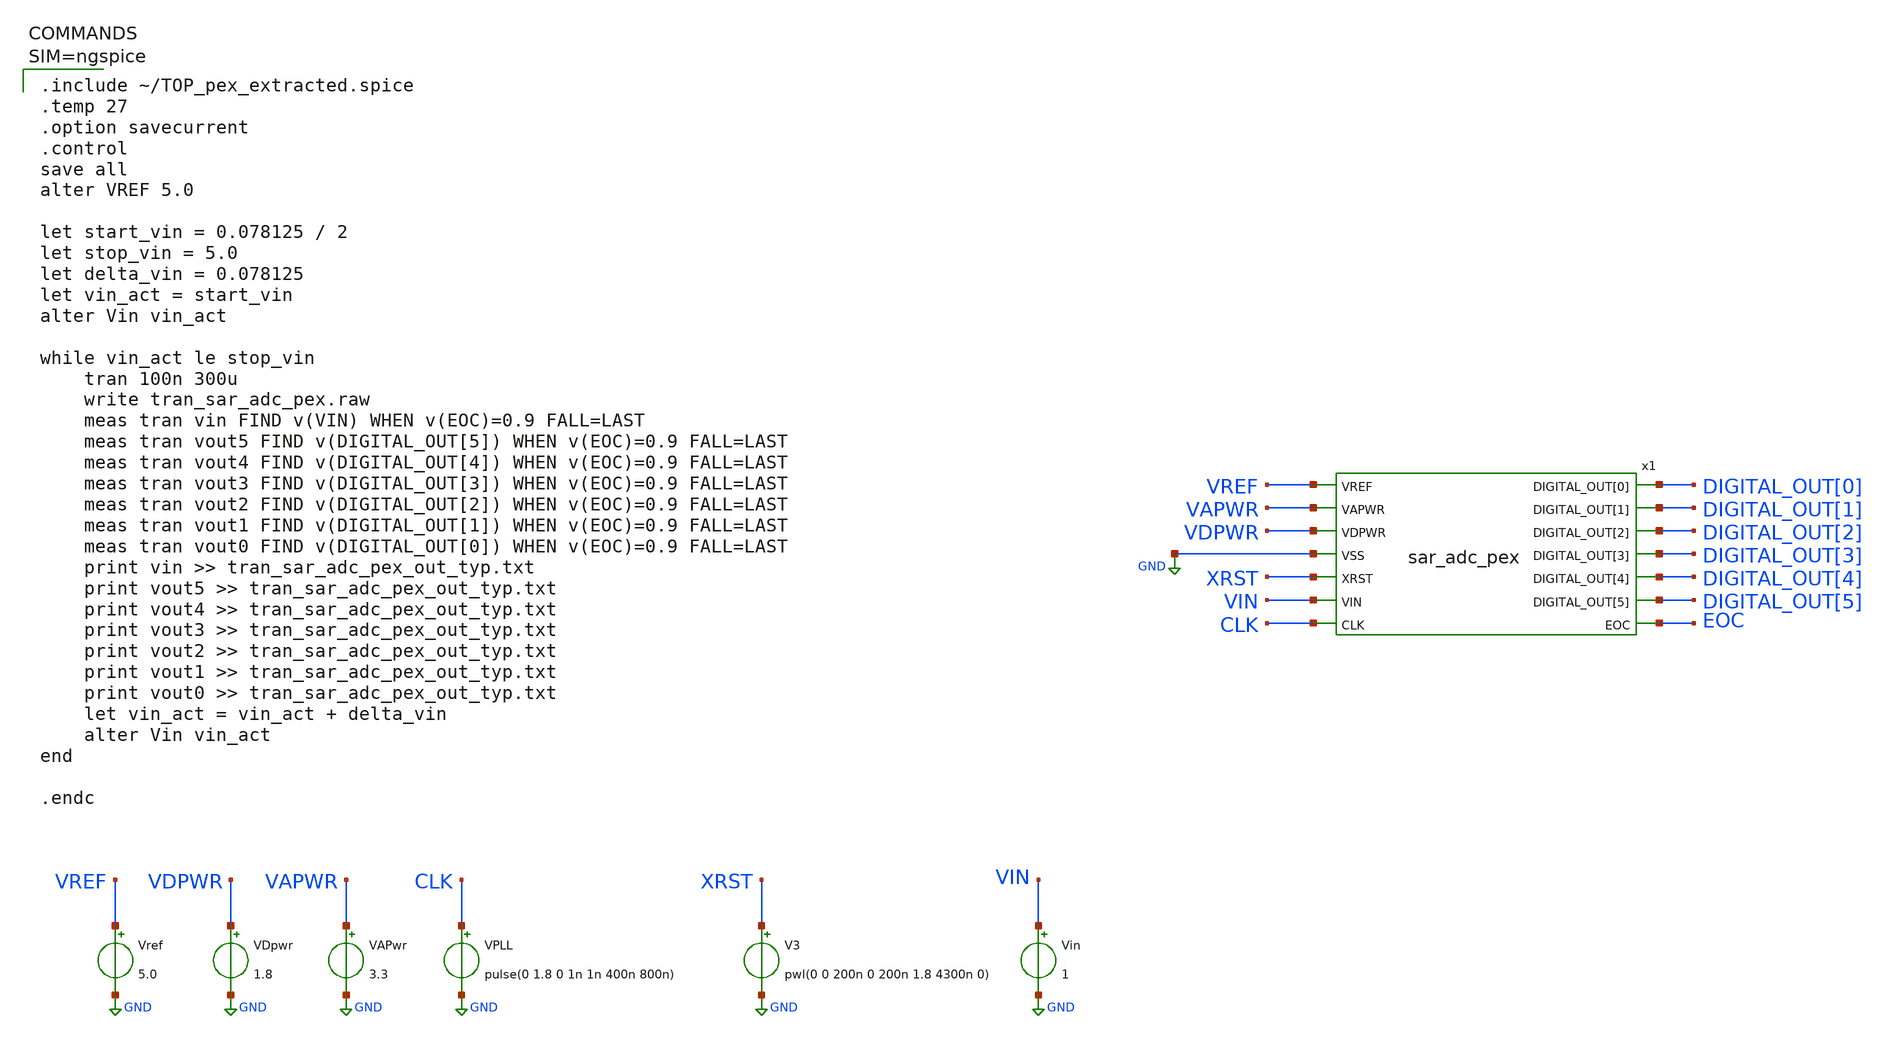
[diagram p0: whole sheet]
** sch_path: SKY130/SAR-ADC/SAR-ADC_5.0V/tran_sar_adc_pex.sch
**.subckt tran_sar_adc_pex
x1 XRST VIN CLK GND DIGITAL_OUT[0] DIGITAL_OUT[1] DIGITAL_OUT[2] DIGITAL_OUT[3] DIGITAL_OUT[4]
+ DIGITAL_OUT[5] EOC TOP
VAPwr VAPWR GND 3.3
Vin VIN GND 1
Vref VREF GND 5.0
VDpwr VDPWR GND 1.8
VPLL CLK GND pulse(0 1.8 0 1n 1n 400n 800n)
V3 XRST GND pwl(0 0 200n 0 200n 1.8 4300n 0)
**** begin user architecture code


.include ~/TOP_pex_extracted.spice
.temp 27
.option savecurrent
.control
save all
alter VREF 5.0

let start_vin = 0.078125 / 2
let stop_vin = 5.0
let delta_vin = 0.078125
let vin_act = start_vin
alter Vin vin_act

while vin_act le stop_vin
	tran 100n 300u
	write tran_sar_adc_pex.raw
	meas tran vin FIND v(VIN) WHEN v(EOC)=0.9 FALL=LAST
	meas tran vout5 FIND v(DIGITAL_OUT[5]) WHEN v(EOC)=0.9 FALL=LAST
	meas tran vout4 FIND v(DIGITAL_OUT[4]) WHEN v(EOC)=0.9 FALL=LAST
	meas tran vout3 FIND v(DIGITAL_OUT[3]) WHEN v(EOC)=0.9 FALL=LAST
	meas tran vout2 FIND v(DIGITAL_OUT[2]) WHEN v(EOC)=0.9 FALL=LAST
	meas tran vout1 FIND v(DIGITAL_OUT[1]) WHEN v(EOC)=0.9 FALL=LAST
	meas tran vout0 FIND v(DIGITAL_OUT[0]) WHEN v(EOC)=0.9 FALL=LAST
	print vin >> tran_sar_adc_pex_out_typ.txt
	print vout5 >> tran_sar_adc_pex_out_typ.txt
	print vout4 >> tran_sar_adc_pex_out_typ.txt
	print vout3 >> tran_sar_adc_pex_out_typ.txt
	print vout2 >> tran_sar_adc_pex_out_typ.txt
	print vout1 >> tran_sar_adc_pex_out_typ.txt
	print vout0 >> tran_sar_adc_pex_out_typ.txt
	let vin_act = vin_act + delta_vin
	alter Vin vin_act
end

.endc




** opencircuitdesign pdks install
.lib $::SKYWATER_MODELS/sky130.lib.spice tt

**** end user architecture code
**.ends
.GLOBAL GND
.end
